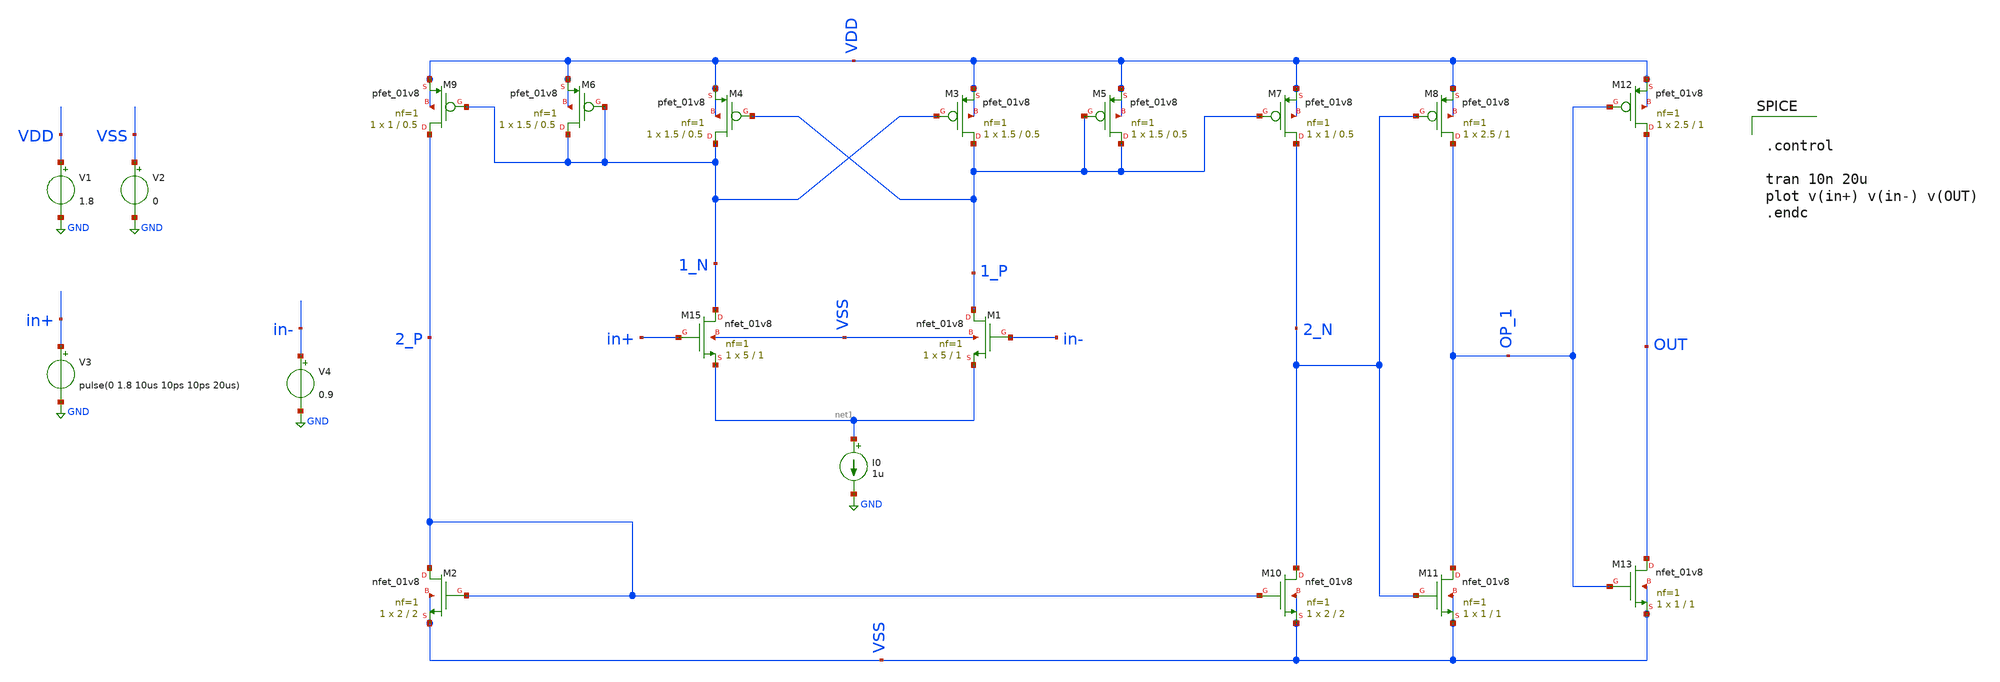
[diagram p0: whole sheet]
** sch_path: xschem/DC_DC_Converter_xschem/OTHERS/DC_DC_Converter0/Comparator/Comparator.sch
**.subckt Comparator
I0 net1 GND 1u
V1 VDD GND 1.8
V2 VSS GND 0
V3 in+ GND pulse(0 1.8 10us 10ps 10ps 20us)
V4 in- GND 0.9
XM15 1_N in+ net1 VSS sky130_fd_pr__nfet_01v8 L=1 W=5 nf=1 ad='int((nf+1)/2) * W/nf * 0.29' as='int((nf+2)/2) * W/nf * 0.29'
+ pd='2*int((nf+1)/2) * (W/nf + 0.29)' ps='2*int((nf+2)/2) * (W/nf + 0.29)' nrd='0.29 / W' nrs='0.29 / W'
+ sa=0 sb=0 sd=0 mult=1 m=1
XM1 1_P in- net1 VSS sky130_fd_pr__nfet_01v8 L=1 W=5 nf=1 ad='int((nf+1)/2) * W/nf * 0.29' as='int((nf+2)/2) * W/nf * 0.29'
+ pd='2*int((nf+1)/2) * (W/nf + 0.29)' ps='2*int((nf+2)/2) * (W/nf + 0.29)' nrd='0.29 / W' nrs='0.29 / W'
+ sa=0 sb=0 sd=0 mult=1 m=1
XM2 2_P 2_P VSS VSS sky130_fd_pr__nfet_01v8 L=2 W=2 nf=1 ad='int((nf+1)/2) * W/nf * 0.29' as='int((nf+2)/2) * W/nf * 0.29'
+ pd='2*int((nf+1)/2) * (W/nf + 0.29)' ps='2*int((nf+2)/2) * (W/nf + 0.29)' nrd='0.29 / W' nrs='0.29 / W'
+ sa=0 sb=0 sd=0 mult=1 m=1
XM10 2_N 2_P VSS VSS sky130_fd_pr__nfet_01v8 L=2 W=2 nf=1 ad='int((nf+1)/2) * W/nf * 0.29' as='int((nf+2)/2) * W/nf * 0.29'
+ pd='2*int((nf+1)/2) * (W/nf + 0.29)' ps='2*int((nf+2)/2) * (W/nf + 0.29)' nrd='0.29 / W' nrs='0.29 / W'
+ sa=0 sb=0 sd=0 mult=1 m=1
XM11 OP_1 2_N VSS VSS sky130_fd_pr__nfet_01v8 L=1 W=1 nf=1 ad='int((nf+1)/2) * W/nf * 0.29' as='int((nf+2)/2) * W/nf * 0.29'
+ pd='2*int((nf+1)/2) * (W/nf + 0.29)' ps='2*int((nf+2)/2) * (W/nf + 0.29)' nrd='0.29 / W' nrs='0.29 / W'
+ sa=0 sb=0 sd=0 mult=1 m=1
XM13 OUT OP_1 VSS VSS sky130_fd_pr__nfet_01v8 L=1 W=1 nf=1 ad='int((nf+1)/2) * W/nf * 0.29' as='int((nf+2)/2) * W/nf * 0.29'
+ pd='2*int((nf+1)/2) * (W/nf + 0.29)' ps='2*int((nf+2)/2) * (W/nf + 0.29)' nrd='0.29 / W' nrs='0.29 / W'
+ sa=0 sb=0 sd=0 mult=1 m=1
XM9 2_P 1_N VDD VDD sky130_fd_pr__pfet_01v8 L=0.5 W=1 nf=1 ad='int((nf+1)/2) * W/nf * 0.29' as='int((nf+2)/2) * W/nf * 0.29'
+ pd='2*int((nf+1)/2) * (W/nf + 0.29)' ps='2*int((nf+2)/2) * (W/nf + 0.29)' nrd='0.29 / W' nrs='0.29 / W'
+ sa=0 sb=0 sd=0 mult=1 m=1
XM6 1_N 1_N VDD VDD sky130_fd_pr__pfet_01v8 L=0.5 W=1.5 nf=1 ad='int((nf+1)/2) * W/nf * 0.29' as='int((nf+2)/2) * W/nf * 0.29'
+ pd='2*int((nf+1)/2) * (W/nf + 0.29)' ps='2*int((nf+2)/2) * (W/nf + 0.29)' nrd='0.29 / W' nrs='0.29 / W'
+ sa=0 sb=0 sd=0 mult=1 m=1
XM4 1_N 1_P VDD VDD sky130_fd_pr__pfet_01v8 L=0.5 W=1.5 nf=1 ad='int((nf+1)/2) * W/nf * 0.29' as='int((nf+2)/2) * W/nf * 0.29'
+ pd='2*int((nf+1)/2) * (W/nf + 0.29)' ps='2*int((nf+2)/2) * (W/nf + 0.29)' nrd='0.29 / W' nrs='0.29 / W'
+ sa=0 sb=0 sd=0 mult=1 m=1
XM3 1_P 1_N VDD VDD sky130_fd_pr__pfet_01v8 L=0.5 W=1.5 nf=1 ad='int((nf+1)/2) * W/nf * 0.29' as='int((nf+2)/2) * W/nf * 0.29'
+ pd='2*int((nf+1)/2) * (W/nf + 0.29)' ps='2*int((nf+2)/2) * (W/nf + 0.29)' nrd='0.29 / W' nrs='0.29 / W'
+ sa=0 sb=0 sd=0 mult=1 m=1
XM5 1_P 1_P VDD VDD sky130_fd_pr__pfet_01v8 L=0.5 W=1.5 nf=1 ad='int((nf+1)/2) * W/nf * 0.29' as='int((nf+2)/2) * W/nf * 0.29'
+ pd='2*int((nf+1)/2) * (W/nf + 0.29)' ps='2*int((nf+2)/2) * (W/nf + 0.29)' nrd='0.29 / W' nrs='0.29 / W'
+ sa=0 sb=0 sd=0 mult=1 m=1
XM7 2_N 1_P VDD VDD sky130_fd_pr__pfet_01v8 L=0.5 W=1 nf=1 ad='int((nf+1)/2) * W/nf * 0.29' as='int((nf+2)/2) * W/nf * 0.29'
+ pd='2*int((nf+1)/2) * (W/nf + 0.29)' ps='2*int((nf+2)/2) * (W/nf + 0.29)' nrd='0.29 / W' nrs='0.29 / W'
+ sa=0 sb=0 sd=0 mult=1 m=1
XM8 OP_1 2_N VDD VDD sky130_fd_pr__pfet_01v8 L=1 W=2.5 nf=1 ad='int((nf+1)/2) * W/nf * 0.29' as='int((nf+2)/2) * W/nf * 0.29'
+ pd='2*int((nf+1)/2) * (W/nf + 0.29)' ps='2*int((nf+2)/2) * (W/nf + 0.29)' nrd='0.29 / W' nrs='0.29 / W'
+ sa=0 sb=0 sd=0 mult=1 m=1
XM12 OUT OP_1 VDD VDD sky130_fd_pr__pfet_01v8 L=1 W=2.5 nf=1 ad='int((nf+1)/2) * W/nf * 0.29' as='int((nf+2)/2) * W/nf * 0.29'
+ pd='2*int((nf+1)/2) * (W/nf + 0.29)' ps='2*int((nf+2)/2) * (W/nf + 0.29)' nrd='0.29 / W' nrs='0.29 / W'
+ sa=0 sb=0 sd=0 mult=1 m=1
**** begin user architecture code


.control

tran 10n 20u
plot v(in+) v(in-) v(OUT)
.endc



** opencircuitdesign pdks install
.lib $::SKYWATER_MODELS/sky130.lib.spice tt


**** end user architecture code
**.ends
.GLOBAL GND
.end
